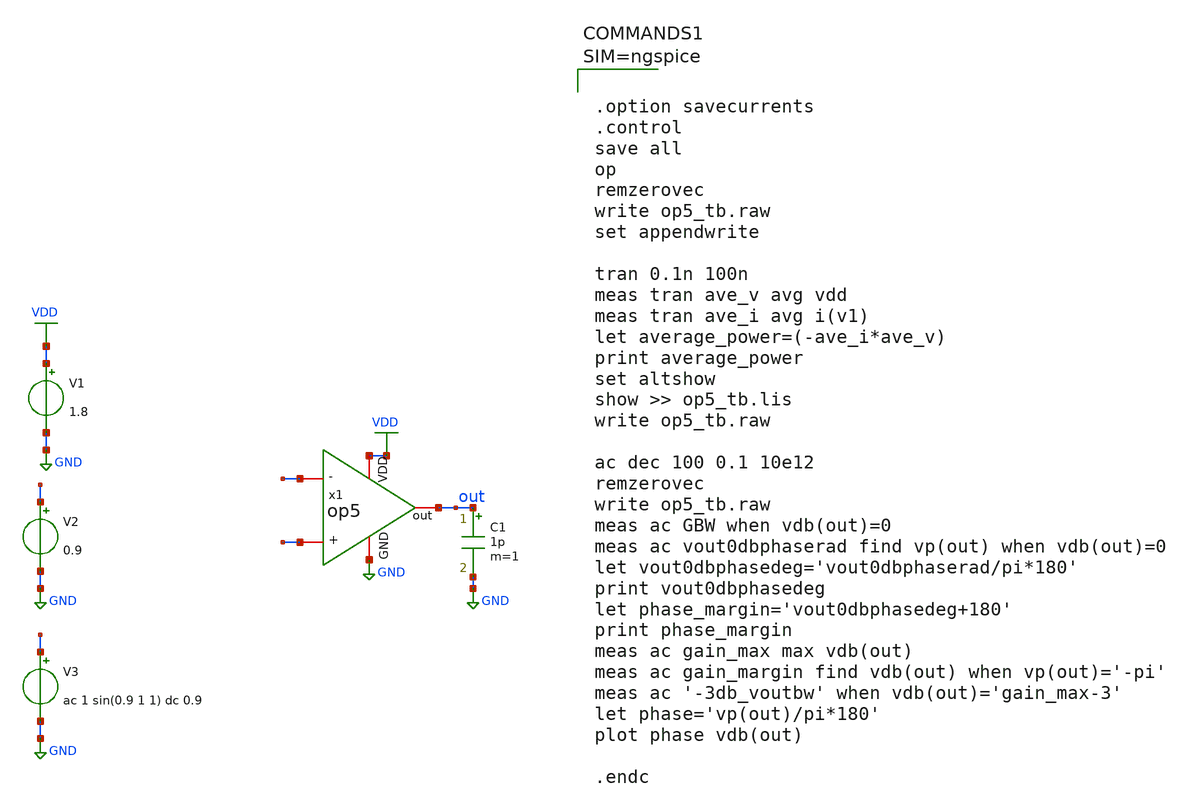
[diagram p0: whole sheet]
** sch_path: xschem/op5.1_tb.sch
**.subckt op5.1_tb
V1 VDD GND 1.8
V2 - GND 0.9
V3 + GND ac 1 sin(0.9 1 1) dc 0.9
C1 out GND 1p m=1
x1 VDD out - + GND op5
**** begin user architecture code

** opencircuitdesign pdks install
.lib $::SKYWATER_MODELS/sky130.lib.spice tt





.option savecurrents
.control
save all
op
remzerovec
write op5_tb.raw
set appendwrite

tran 0.1n 100n
meas tran ave_v avg vdd
meas tran ave_i avg i(v1)
let average_power=(-ave_i*ave_v)
print average_power
set altshow
show >> op5_tb.lis
write op5_tb.raw

ac dec 100 0.1 10e12
remzerovec
write op5_tb.raw
meas ac GBW when vdb(out)=0
meas ac vout0dbphaserad find vp(out) when vdb(out)=0
let vout0dbphasedeg='vout0dbphaserad/pi*180'
print vout0dbphasedeg
let phase_margin='vout0dbphasedeg+180'
print phase_margin
meas ac gain_max max vdb(out)
meas ac gain_margin find vdb(out) when vp(out)='-pi'
meas ac '-3db_voutbw' when vdb(out)='gain_max-3'
let phase='vp(out)/pi*180'
plot phase vdb(out)

.endc



**** end user architecture code
**.ends

* expanding   symbol:  op5.sym # of pins=5
** sym_path: xschem/op5.sym
** sch_path: xschem/op5.sch
.subckt op5 VDD out - + GND
*.iopin VDD
*.iopin GND
*.iopin -
*.iopin +
*.iopin out
C2 out net5 2.2p m=1
R2 net5 net1 1k m=1
XM1 bias bias net6 GND sky130_fd_pr__nfet_01v8 L={L5} W={W5} nf=1 ad='int((nf+1)/2) * W/nf * 0.29' as='int((nf+2)/2) * W/nf * 0.29'
+ pd='2*int((nf+1)/2) * (W/nf + 0.29)' ps='2*int((nf+2)/2) * (W/nf + 0.29)' nrd='0.29 / W' nrs='0.29 / W'
+ sa=0 sb=0 sd=0 mult=4 m=4
XM2 net4 bias GND GND sky130_fd_pr__nfet_01v8 L={L5} W={W5} nf=1 ad='int((nf+1)/2) * W/nf * 0.29' as='int((nf+2)/2) * W/nf * 0.29'
+ pd='2*int((nf+1)/2) * (W/nf + 0.29)' ps='2*int((nf+2)/2) * (W/nf + 0.29)' nrd='0.29 / W' nrs='0.29 / W'
+ sa=0 sb=0 sd=0 mult=4 m=4
XM3 net2 - net3 GND sky130_fd_pr__nfet_01v8 L={L4} W={W4} nf=1 ad='int((nf+1)/2) * W/nf * 0.29' as='int((nf+2)/2) * W/nf * 0.29'
+ pd='2*int((nf+1)/2) * (W/nf + 0.29)' ps='2*int((nf+2)/2) * (W/nf + 0.29)' nrd='0.29 / W' nrs='0.29 / W'
+ sa=0 sb=0 sd=0 mult=4 m=4
XM4 net1 + net3 GND sky130_fd_pr__nfet_01v8 L={L4} W={W4} nf=1 ad='int((nf+1)/2) * W/nf * 0.29' as='int((nf+2)/2) * W/nf * 0.29'
+ pd='2*int((nf+1)/2) * (W/nf + 0.29)' ps='2*int((nf+2)/2) * (W/nf + 0.29)' nrd='0.29 / W' nrs='0.29 / W'
+ sa=0 sb=0 sd=0 mult=4 m=4
XM6 bias net4 VDD VDD sky130_fd_pr__pfet_01v8 L={L1} W={W1} nf=1 ad='int((nf+1)/2) * W/nf * 0.29' as='int((nf+2)/2) * W/nf * 0.29'
+ pd='2*int((nf+1)/2) * (W/nf + 0.29)' ps='2*int((nf+2)/2) * (W/nf + 0.29)' nrd='0.29 / W' nrs='0.29 / W'
+ sa=0 sb=0 sd=0 mult=4 m=4
XM7 net4 net4 VDD VDD sky130_fd_pr__pfet_01v8 L={L1} W={W1} nf=1 ad='int((nf+1)/2) * W/nf * 0.29' as='int((nf+2)/2) * W/nf * 0.29'
+ pd='2*int((nf+1)/2) * (W/nf + 0.29)' ps='2*int((nf+2)/2) * (W/nf + 0.29)' nrd='0.29 / W' nrs='0.29 / W'
+ sa=0 sb=0 sd=0 mult=4 m=4
XM8 net1 net2 VDD VDD sky130_fd_pr__pfet_01v8 L={L7} W={W7} nf=1 ad='int((nf+1)/2) * W/nf * 0.29' as='int((nf+2)/2) * W/nf * 0.29'
+ pd='2*int((nf+1)/2) * (W/nf + 0.29)' ps='2*int((nf+2)/2) * (W/nf + 0.29)' nrd='0.29 / W' nrs='0.29 / W'
+ sa=0 sb=0 sd=0 mult=4 m=4
XM9 net2 net2 VDD VDD sky130_fd_pr__pfet_01v8 L={L7} W={W7} nf=1 ad='int((nf+1)/2) * W/nf * 0.29' as='int((nf+2)/2) * W/nf * 0.29'
+ pd='2*int((nf+1)/2) * (W/nf + 0.29)' ps='2*int((nf+2)/2) * (W/nf + 0.29)' nrd='0.29 / W' nrs='0.29 / W'
+ sa=0 sb=0 sd=0 mult=4 m=4
XM5 net3 bias GND GND sky130_fd_pr__nfet_01v8 L={L6} W={W6} nf=1 ad='int((nf+1)/2) * W/nf * 0.29' as='int((nf+2)/2) * W/nf * 0.29'
+ pd='2*int((nf+1)/2) * (W/nf + 0.29)' ps='2*int((nf+2)/2) * (W/nf + 0.29)' nrd='0.29 / W' nrs='0.29 / W'
+ sa=0 sb=0 sd=0 mult=4 m=4
XM10 out net1 VDD VDD sky130_fd_pr__pfet_01v8 L={L2} W={W2} nf=1 ad='int((nf+1)/2) * W/nf * 0.29' as='int((nf+2)/2) * W/nf * 0.29'
+ pd='2*int((nf+1)/2) * (W/nf + 0.29)' ps='2*int((nf+2)/2) * (W/nf + 0.29)' nrd='0.29 / W' nrs='0.29 / W'
+ sa=0 sb=0 sd=0 mult=4 m=4
XM11 out bias GND GND sky130_fd_pr__nfet_01v8 L={L3} W={W3} nf=1 ad='int((nf+1)/2) * W/nf * 0.29' as='int((nf+2)/2) * W/nf * 0.29'
+ pd='2*int((nf+1)/2) * (W/nf + 0.29)' ps='2*int((nf+2)/2) * (W/nf + 0.29)' nrd='0.29 / W' nrs='0.29 / W'
+ sa=0 sb=0 sd=0 mult=4 m=4
R3 net6 GND 5k m=1
**** begin user architecture code


**************
*PMOS cms
.param L1=2.7
.param W1=1.25

**************
*NMOS cms
.param L5=2
.param W5=3.5

**************
*PMOS current differential
.param L7=2.7
.param W7=1.25

**************
*differential Pair
.param L4=2.7
.param W4=1.25

**************
*NMOS current control
.param L6=2
.param W6=3.5

**************
*Second Stage
.param L2=2
.param W2=3.5

**************
*NMOS current second stage
.param L3=2
.param W3=3.5


**** end user architecture code
.ends

.GLOBAL VDD
.GLOBAL GND
.end
